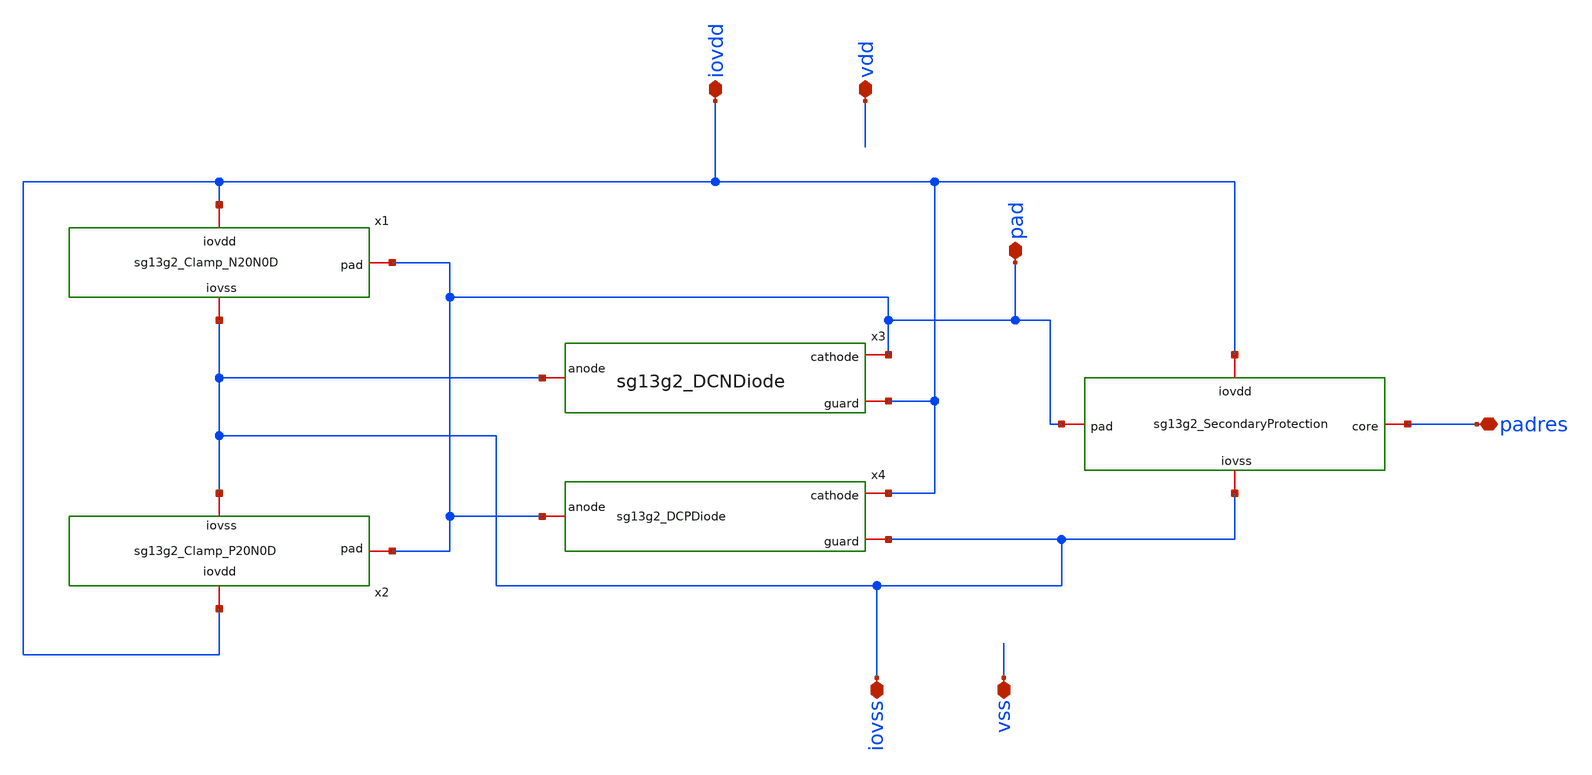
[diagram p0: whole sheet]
** sch_path: ihp-sg13g2/libs.ref/sg13g2_io/xschem/sg13g2_IOPadAnalog.sch
**.subckt sg13g2_IOPadAnalog padres iovss iovdd pad vdd vss
*.iopin padres
*.iopin iovss
*.iopin iovdd
*.iopin pad
*.iopin vdd
*.iopin vss
x3 pad iovss iovdd sg13g2_DCNDiode
x4 iovdd pad iovss sg13g2_DCPDiode
x1 iovdd pad padres iovss sg13g2_SecondaryProtection
x1 pad iovdd iovss sg13g2_Clamp_N20N0D
x2 iovdd pad iovss sg13g2_Clamp_P20N0D
**.ends

* expanding   symbol:  sg13g2_DCNDiode.sym # of pins=3
** sym_path: ihp-sg13g2/libs.ref/sg13g2_io/xschem/sg13g2_DCNDiode.sym
** sch_path: ihp-sg13g2/libs.ref/sg13g2_io/xschem/sg13g2_DCNDiode.sch
.subckt sg13g2_DCNDiode cathode anode guard
*.iopin cathode
*.iopin anode
*.iopin guard
XD1 anode cathode dantenna l=1.26u w=27.78u
XD2 anode cathode dantenna l=1.26u w=27.78u
.ends


* expanding   symbol:  sg13g2_DCPDiode.sym # of pins=3
** sym_path: ihp-sg13g2/libs.ref/sg13g2_io/xschem/sg13g2_DCPDiode.sym
** sch_path: ihp-sg13g2/libs.ref/sg13g2_io/xschem/sg13g2_DCPDiode.sch
.subckt sg13g2_DCPDiode cathode anode guard
*.iopin cathode
*.iopin anode
*.iopin guard
XD1 anode cathode dpantenna l=1.26u w=27.78u
XD2 anode cathode dpantenna l=1.26u w=27.78u
.ends


* expanding   symbol:  sg13g2_SecondaryProtection.sym # of pins=4
** sym_path: ihp-sg13g2/libs.ref/sg13g2_io/xschem/sg13g2_SecondaryProtection.sym
** sch_path: ihp-sg13g2/libs.ref/sg13g2_io/xschem/sg13g2_SecondaryProtection.sch
.subckt sg13g2_SecondaryProtection iovdd pad core iovss
*.iopin iovdd
*.iopin iovss
*.iopin core
*.iopin pad
XR1 core pad sub! rppd w=1e-6 l=2e-6 m=1 b=0 mm_ok=1
XD1 iovss core dantenna l=3.1u w=0.64u
XD2 core iovdd dpantenna l=0.64u w=4.98u
.ends


* expanding   symbol:  sg13g2_Clamp_N20N0D.sym # of pins=3
** sym_path: ihp-sg13g2/libs.ref/sg13g2_io/xschem/sg13g2_Clamp_N20N0D.sym
** sch_path: ihp-sg13g2/libs.ref/sg13g2_io/xschem/sg13g2_Clamp_N20N0D.sch
.subckt sg13g2_Clamp_N20N0D pad iovdd iovss
*.iopin iovss
*.iopin pad
*.iopin iovdd
XM1 iovss net1 pad iovss sg13_hv_nmos w=4.4u l=0.6u ng=1 m=1 mm_ok=1
XM2 iovss net1 pad iovss sg13_hv_nmos w=4.4u l=0.6u ng=1 m=1 mm_ok=1
XM3 iovss net1 pad iovss sg13_hv_nmos w=4.4u l=0.6u ng=1 m=1 mm_ok=1
XM4 iovss net1 pad iovss sg13_hv_nmos w=4.4u l=0.6u ng=1 m=1 mm_ok=1
XM5 iovss net1 pad iovss sg13_hv_nmos w=4.4u l=0.6u ng=1 m=1 mm_ok=1
XM6 iovss net1 pad iovss sg13_hv_nmos w=4.4u l=0.6u ng=1 m=1 mm_ok=1
XM7 iovss net1 pad iovss sg13_hv_nmos w=4.4u l=0.6u ng=1 m=1 mm_ok=1
XM8 iovss net1 pad iovss sg13_hv_nmos w=4.4u l=0.6u ng=1 m=1 mm_ok=1
XM9 iovss net1 pad iovss sg13_hv_nmos w=4.4u l=0.6u ng=1 m=1 mm_ok=1
XM10 iovss net1 pad iovss sg13_hv_nmos w=4.4u l=0.6u ng=1 m=1 mm_ok=1
XM11 iovss net1 pad iovss sg13_hv_nmos w=4.4u l=0.6u ng=1 m=1 mm_ok=1
XM12 iovss net1 pad iovss sg13_hv_nmos w=4.4u l=0.6u ng=1 m=1 mm_ok=1
XM13 iovss net1 pad iovss sg13_hv_nmos w=4.4u l=0.6u ng=1 m=1 mm_ok=1
XM14 iovss net1 pad iovss sg13_hv_nmos w=4.4u l=0.6u ng=1 m=1 mm_ok=1
XM15 iovss net1 pad iovss sg13_hv_nmos w=4.4u l=0.6u ng=1 m=1 mm_ok=1
XM16 iovss net1 pad iovss sg13_hv_nmos w=4.4u l=0.6u ng=1 m=1 mm_ok=1
XM17 iovss net1 pad iovss sg13_hv_nmos w=4.4u l=0.6u ng=1 m=1 mm_ok=1
XM18 iovss net1 pad iovss sg13_hv_nmos w=4.4u l=0.6u ng=1 m=1 mm_ok=1
XM19 iovss net1 pad iovss sg13_hv_nmos w=4.4u l=0.6u ng=1 m=1 mm_ok=1
XM20 iovss net1 pad iovss sg13_hv_nmos w=4.4u l=0.6u ng=1 m=1 mm_ok=1
XRp1 net1 iovss sub! rppd w=0.5e-6 l=3.54e-6 m=1 b=0 mm_ok=1
.ends


* expanding   symbol:  sg13g2_Clamp_P20N0D.sym # of pins=3
** sym_path: ihp-sg13g2/libs.ref/sg13g2_io/xschem/sg13g2_Clamp_P20N0D.sym
** sch_path: ihp-sg13g2/libs.ref/sg13g2_io/xschem/sg13g2_Clamp_P20N0D.sch
.subckt sg13g2_Clamp_P20N0D iovdd pad iovss
*.iopin iovdd
*.iopin pad
*.iopin iovss
XM1 pad net1 iovdd iovdd sg13_hv_pmos w=6.66u l=0.6u ng=1 m=1 mm_ok=1
XM2 pad net1 iovdd iovdd sg13_hv_pmos w=6.66u l=0.6u ng=1 m=1 mm_ok=1
XM3 pad net1 iovdd net2 sg13_hv_pmos w=6.66u l=0.6u ng=1 m=1 mm_ok=1
XM4 pad net1 iovdd iovdd sg13_hv_pmos w=6.66u l=0.6u ng=1 m=1 mm_ok=1
XM5 pad net1 iovdd net3 sg13_hv_pmos w=6.66u l=0.6u ng=1 m=1 mm_ok=1
XM6 pad net1 iovdd net4 sg13_hv_pmos w=6.66u l=0.6u ng=1 m=1 mm_ok=1
XM7 pad net1 iovdd net5 sg13_hv_pmos w=6.66u l=0.6u ng=1 m=1 mm_ok=1
XM8 pad net1 iovdd iovdd sg13_hv_pmos w=6.66u l=0.6u ng=1 m=1 mm_ok=1
XM9 pad net1 iovdd iovdd sg13_hv_pmos w=6.66u l=0.6u ng=1 m=1 mm_ok=1
XM10 pad net1 iovdd iovdd sg13_hv_pmos w=6.66u l=0.6u ng=1 m=1 mm_ok=1
XM11 pad net1 iovdd iovdd sg13_hv_pmos w=6.66u l=0.6u ng=1 m=1 mm_ok=1
XM12 pad net1 iovdd iovdd sg13_hv_pmos w=6.66u l=0.6u ng=1 m=1 mm_ok=1
XM13 pad net1 iovdd iovdd sg13_hv_pmos w=6.66u l=0.6u ng=1 m=1 mm_ok=1
XM14 pad net1 iovdd iovdd sg13_hv_pmos w=6.66u l=0.6u ng=1 m=1 mm_ok=1
XM15 pad net1 iovdd iovdd sg13_hv_pmos w=6.66u l=0.6u ng=1 m=1 mm_ok=1
XM16 pad net1 iovdd iovdd sg13_hv_pmos w=6.66u l=0.6u ng=1 m=1 mm_ok=1
XM17 pad net1 iovdd iovdd sg13_hv_pmos w=6.66u l=0.6u ng=1 m=1 mm_ok=1
XM18 pad net1 iovdd iovdd sg13_hv_pmos w=6.66u l=0.6u ng=1 m=1 mm_ok=1
XM19 pad net1 iovdd iovdd sg13_hv_pmos w=6.66u l=0.6u ng=1 m=1 mm_ok=1
XM20 pad net1 iovdd iovdd sg13_hv_pmos w=6.66u l=0.6u ng=1 m=1 mm_ok=1
XM21 pad net1 iovdd iovdd sg13_hv_pmos w=6.66u l=0.6u ng=1 m=1 mm_ok=1
XM22 pad net1 iovdd iovdd sg13_hv_pmos w=6.66u l=0.6u ng=1 m=1 mm_ok=1
XM23 pad net1 iovdd iovdd sg13_hv_pmos w=6.66u l=0.6u ng=1 m=1 mm_ok=1
XM24 pad net1 iovdd iovdd sg13_hv_pmos w=6.66u l=0.6u ng=1 m=1 mm_ok=1
XM25 pad net1 iovdd iovdd sg13_hv_pmos w=6.66u l=0.6u ng=1 m=1 mm_ok=1
XM26 pad net1 iovdd iovdd sg13_hv_pmos w=6.66u l=0.6u ng=1 m=1 mm_ok=1
XM27 pad net1 iovdd iovdd sg13_hv_pmos w=6.66u l=0.6u ng=1 m=1 mm_ok=1
XM28 pad net1 iovdd iovdd sg13_hv_pmos w=6.66u l=0.6u ng=1 m=1 mm_ok=1
XM29 pad net1 iovdd iovdd sg13_hv_pmos w=6.66u l=0.6u ng=1 m=1 mm_ok=1
XM30 pad net1 iovdd iovdd sg13_hv_pmos w=6.66u l=0.6u ng=1 m=1 mm_ok=1
XM31 pad net1 iovdd iovdd sg13_hv_pmos w=6.66u l=0.6u ng=1 m=1 mm_ok=1
XM32 pad net1 iovdd iovdd sg13_hv_pmos w=6.66u l=0.6u ng=1 m=1 mm_ok=1
XM33 pad net1 iovdd iovdd sg13_hv_pmos w=6.66u l=0.6u ng=1 m=1 mm_ok=1
XM34 pad net1 iovdd iovdd sg13_hv_pmos w=6.66u l=0.6u ng=1 m=1 mm_ok=1
XM35 pad net1 iovdd iovdd sg13_hv_pmos w=6.66u l=0.6u ng=1 m=1 mm_ok=1
XM36 pad net1 iovdd iovdd sg13_hv_pmos w=6.66u l=0.6u ng=1 m=1 mm_ok=1
XM37 pad net1 iovdd iovdd sg13_hv_pmos w=6.66u l=0.6u ng=1 m=1 mm_ok=1
XM38 pad net1 iovdd iovdd sg13_hv_pmos w=6.66u l=0.6u ng=1 m=1 mm_ok=1
XM39 pad net1 iovdd iovdd sg13_hv_pmos w=6.66u l=0.6u ng=1 m=1 mm_ok=1
XM40 pad net1 iovdd iovdd sg13_hv_pmos w=6.66u l=0.6u ng=1 m=1 mm_ok=1
XR1 iovdd net1 sub! rppd w=0.5e-6 l=12.9e-6 m=1 b=0 mm_ok=1
.ends

.end
